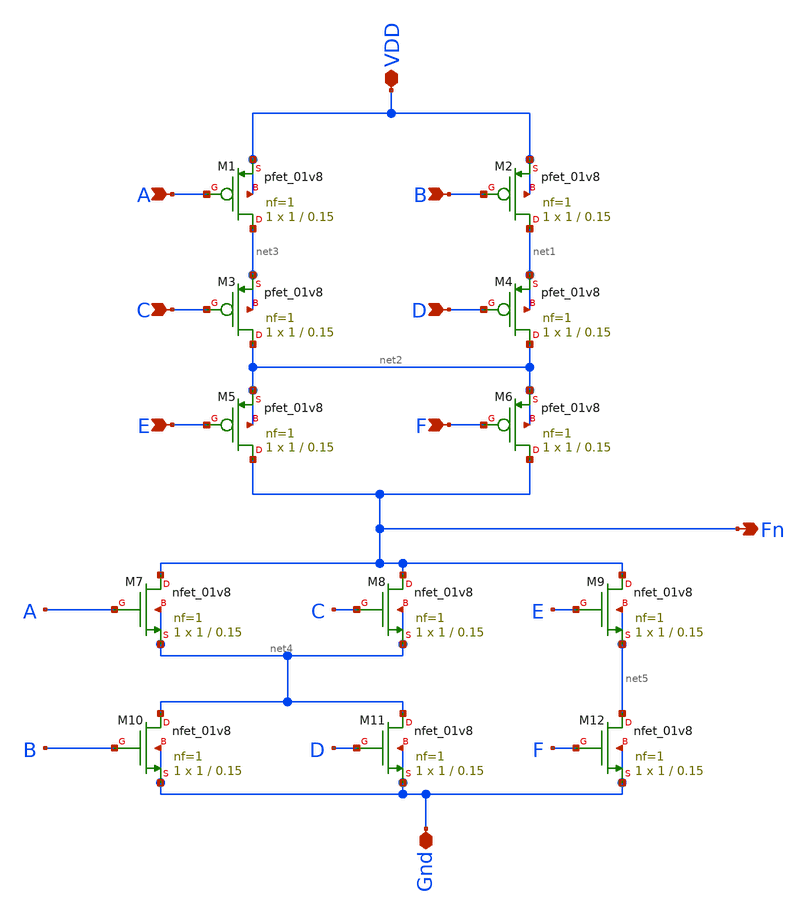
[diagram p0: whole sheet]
** sch_path: Week_1/Function_PreLayout/function_pre_sym.sch
**.subckt function_pre_sym A B C D E F Fn VDD Gnd
*.ipin A
*.ipin B
*.ipin C
*.ipin D
*.ipin E
*.ipin F
*.opin Fn
*.iopin VDD
*.iopin Gnd
XM1 net3 A VDD VDD sky130_fd_pr__pfet_01v8 L=0.15 W=1 nf=1 ad='int((nf+1)/2) * W/nf * 0.29' as='int((nf+2)/2) * W/nf * 0.29'
+ pd='2*int((nf+1)/2) * (W/nf + 0.29)' ps='2*int((nf+2)/2) * (W/nf + 0.29)' nrd='0.29 / W' nrs='0.29 / W'
+ sa=0 sb=0 sd=0 mult=1 m=1
XM2 net1 B VDD VDD sky130_fd_pr__pfet_01v8 L=0.15 W=1 nf=1 ad='int((nf+1)/2) * W/nf * 0.29' as='int((nf+2)/2) * W/nf * 0.29'
+ pd='2*int((nf+1)/2) * (W/nf + 0.29)' ps='2*int((nf+2)/2) * (W/nf + 0.29)' nrd='0.29 / W' nrs='0.29 / W'
+ sa=0 sb=0 sd=0 mult=1 m=1
XM3 net2 C net3 net3 sky130_fd_pr__pfet_01v8 L=0.15 W=1 nf=1 ad='int((nf+1)/2) * W/nf * 0.29' as='int((nf+2)/2) * W/nf * 0.29'
+ pd='2*int((nf+1)/2) * (W/nf + 0.29)' ps='2*int((nf+2)/2) * (W/nf + 0.29)' nrd='0.29 / W' nrs='0.29 / W'
+ sa=0 sb=0 sd=0 mult=1 m=1
XM4 net2 D net1 net1 sky130_fd_pr__pfet_01v8 L=0.15 W=1 nf=1 ad='int((nf+1)/2) * W/nf * 0.29' as='int((nf+2)/2) * W/nf * 0.29'
+ pd='2*int((nf+1)/2) * (W/nf + 0.29)' ps='2*int((nf+2)/2) * (W/nf + 0.29)' nrd='0.29 / W' nrs='0.29 / W'
+ sa=0 sb=0 sd=0 mult=1 m=1
XM5 Fn E net2 net2 sky130_fd_pr__pfet_01v8 L=0.15 W=1 nf=1 ad='int((nf+1)/2) * W/nf * 0.29' as='int((nf+2)/2) * W/nf * 0.29'
+ pd='2*int((nf+1)/2) * (W/nf + 0.29)' ps='2*int((nf+2)/2) * (W/nf + 0.29)' nrd='0.29 / W' nrs='0.29 / W'
+ sa=0 sb=0 sd=0 mult=1 m=1
XM6 Fn F net2 net2 sky130_fd_pr__pfet_01v8 L=0.15 W=1 nf=1 ad='int((nf+1)/2) * W/nf * 0.29' as='int((nf+2)/2) * W/nf * 0.29'
+ pd='2*int((nf+1)/2) * (W/nf + 0.29)' ps='2*int((nf+2)/2) * (W/nf + 0.29)' nrd='0.29 / W' nrs='0.29 / W'
+ sa=0 sb=0 sd=0 mult=1 m=1
XM7 Fn A net4 net4 sky130_fd_pr__nfet_01v8 L=0.15 W=1 nf=1 ad='int((nf+1)/2) * W/nf * 0.29' as='int((nf+2)/2) * W/nf * 0.29'
+ pd='2*int((nf+1)/2) * (W/nf + 0.29)' ps='2*int((nf+2)/2) * (W/nf + 0.29)' nrd='0.29 / W' nrs='0.29 / W'
+ sa=0 sb=0 sd=0 mult=1 m=1
XM8 Fn C net4 net4 sky130_fd_pr__nfet_01v8 L=0.15 W=1 nf=1 ad='int((nf+1)/2) * W/nf * 0.29' as='int((nf+2)/2) * W/nf * 0.29'
+ pd='2*int((nf+1)/2) * (W/nf + 0.29)' ps='2*int((nf+2)/2) * (W/nf + 0.29)' nrd='0.29 / W' nrs='0.29 / W'
+ sa=0 sb=0 sd=0 mult=1 m=1
XM9 Fn E net5 net5 sky130_fd_pr__nfet_01v8 L=0.15 W=1 nf=1 ad='int((nf+1)/2) * W/nf * 0.29' as='int((nf+2)/2) * W/nf * 0.29'
+ pd='2*int((nf+1)/2) * (W/nf + 0.29)' ps='2*int((nf+2)/2) * (W/nf + 0.29)' nrd='0.29 / W' nrs='0.29 / W'
+ sa=0 sb=0 sd=0 mult=1 m=1
XM10 net4 B Gnd Gnd sky130_fd_pr__nfet_01v8 L=0.15 W=1 nf=1 ad='int((nf+1)/2) * W/nf * 0.29' as='int((nf+2)/2) * W/nf * 0.29'
+ pd='2*int((nf+1)/2) * (W/nf + 0.29)' ps='2*int((nf+2)/2) * (W/nf + 0.29)' nrd='0.29 / W' nrs='0.29 / W'
+ sa=0 sb=0 sd=0 mult=1 m=1
XM11 net4 D Gnd Gnd sky130_fd_pr__nfet_01v8 L=0.15 W=1 nf=1 ad='int((nf+1)/2) * W/nf * 0.29' as='int((nf+2)/2) * W/nf * 0.29'
+ pd='2*int((nf+1)/2) * (W/nf + 0.29)' ps='2*int((nf+2)/2) * (W/nf + 0.29)' nrd='0.29 / W' nrs='0.29 / W'
+ sa=0 sb=0 sd=0 mult=1 m=1
XM12 net5 F Gnd Gnd sky130_fd_pr__nfet_01v8 L=0.15 W=1 nf=1 ad='int((nf+1)/2) * W/nf * 0.29' as='int((nf+2)/2) * W/nf * 0.29'
+ pd='2*int((nf+1)/2) * (W/nf + 0.29)' ps='2*int((nf+2)/2) * (W/nf + 0.29)' nrd='0.29 / W' nrs='0.29 / W'
+ sa=0 sb=0 sd=0 mult=1 m=1
**.ends
.end
